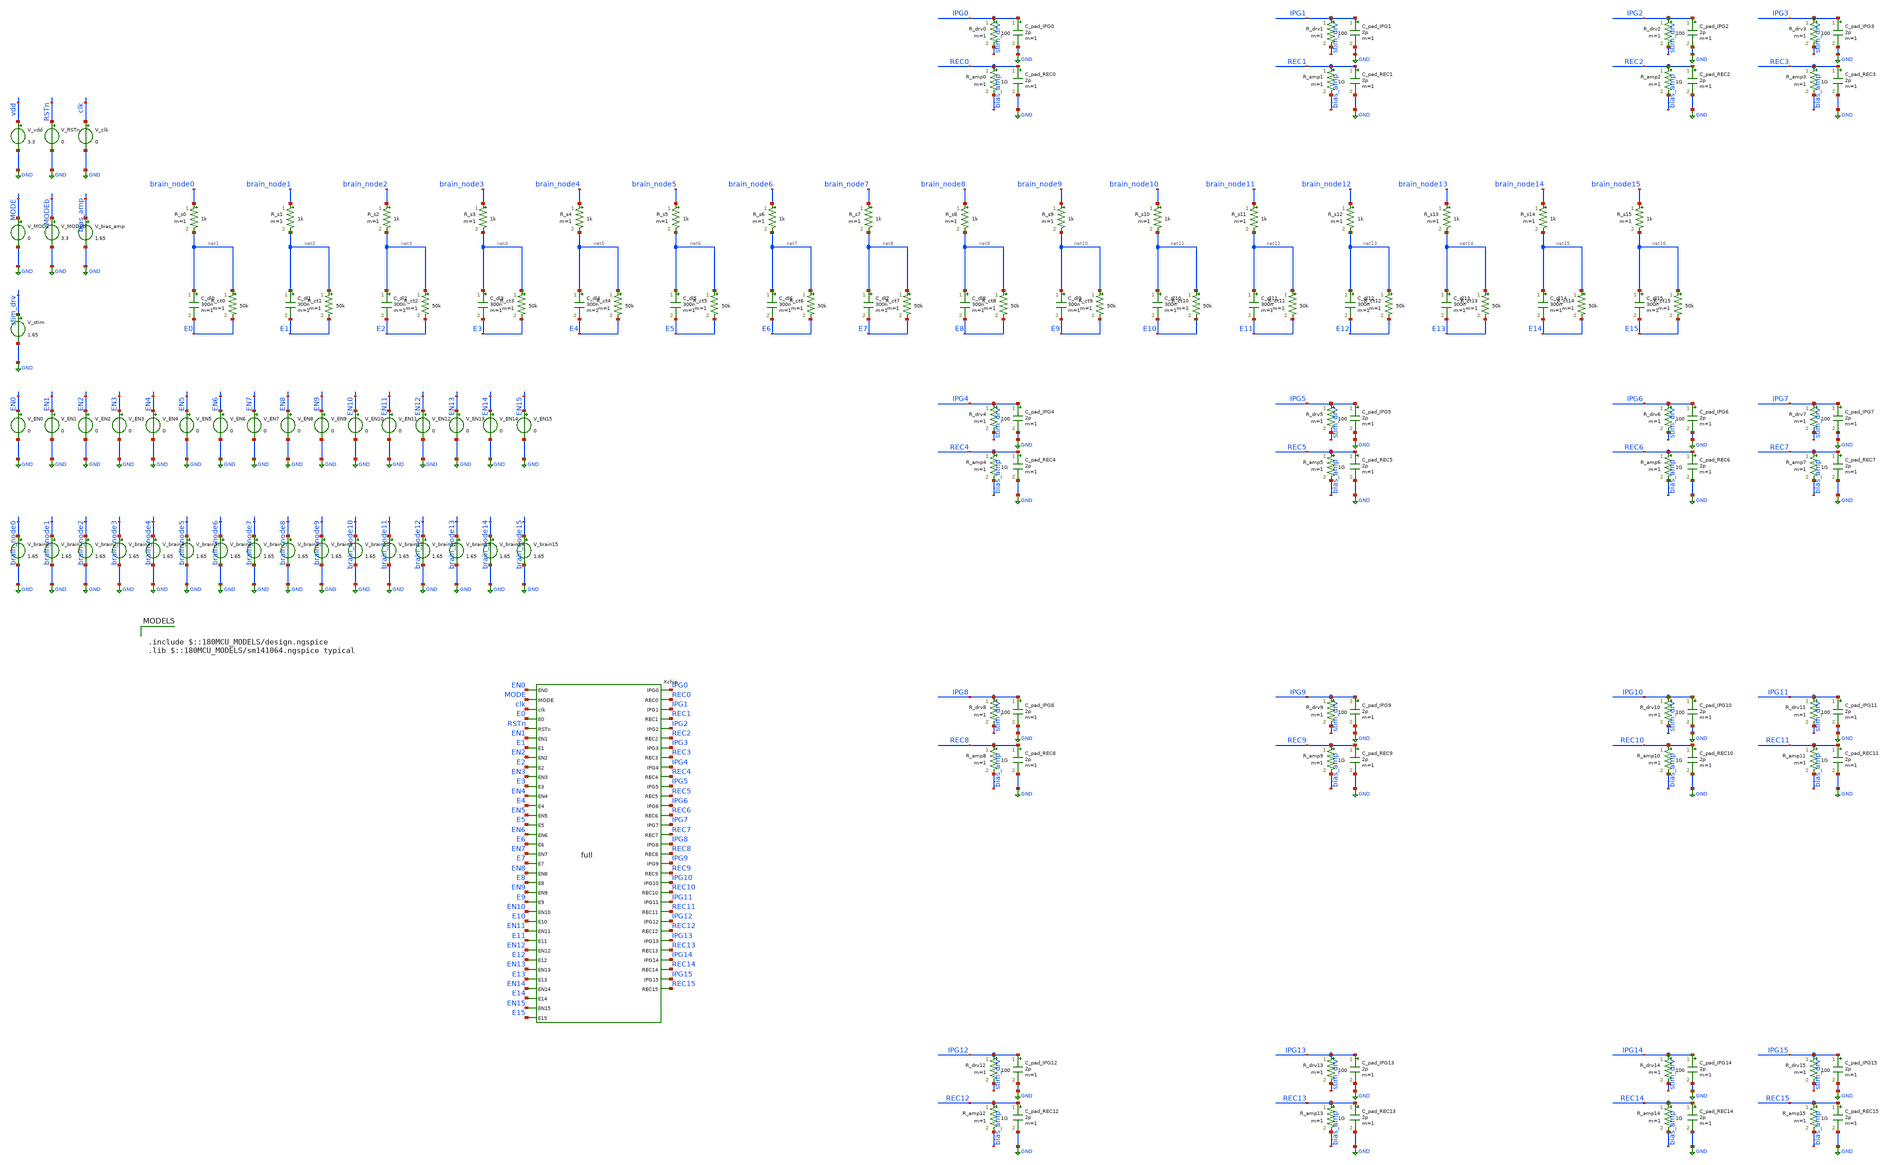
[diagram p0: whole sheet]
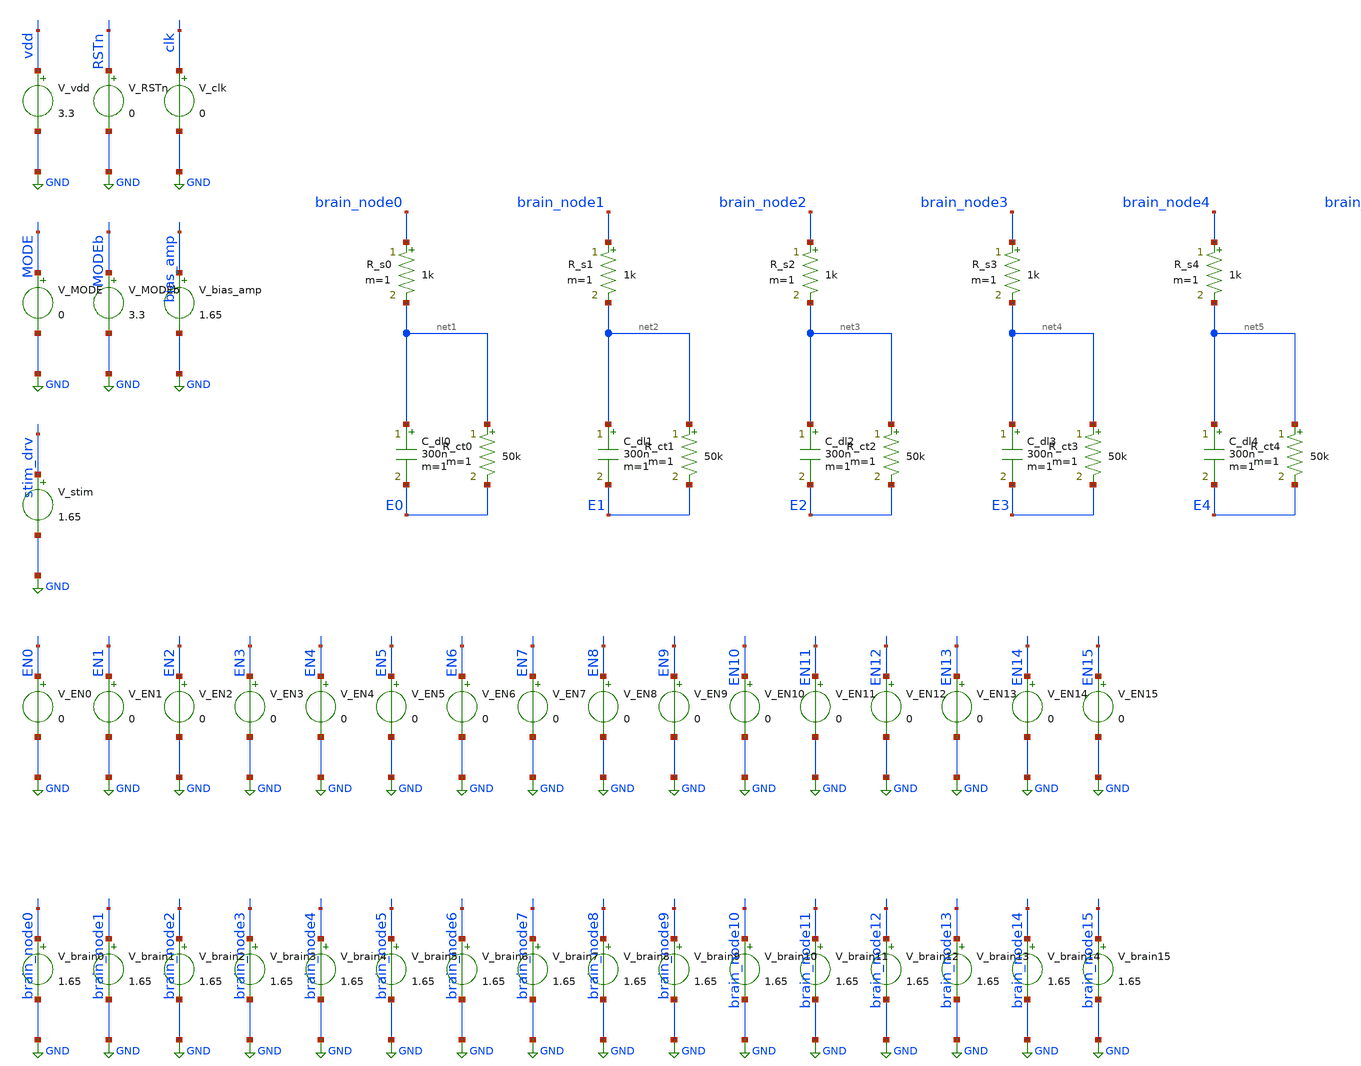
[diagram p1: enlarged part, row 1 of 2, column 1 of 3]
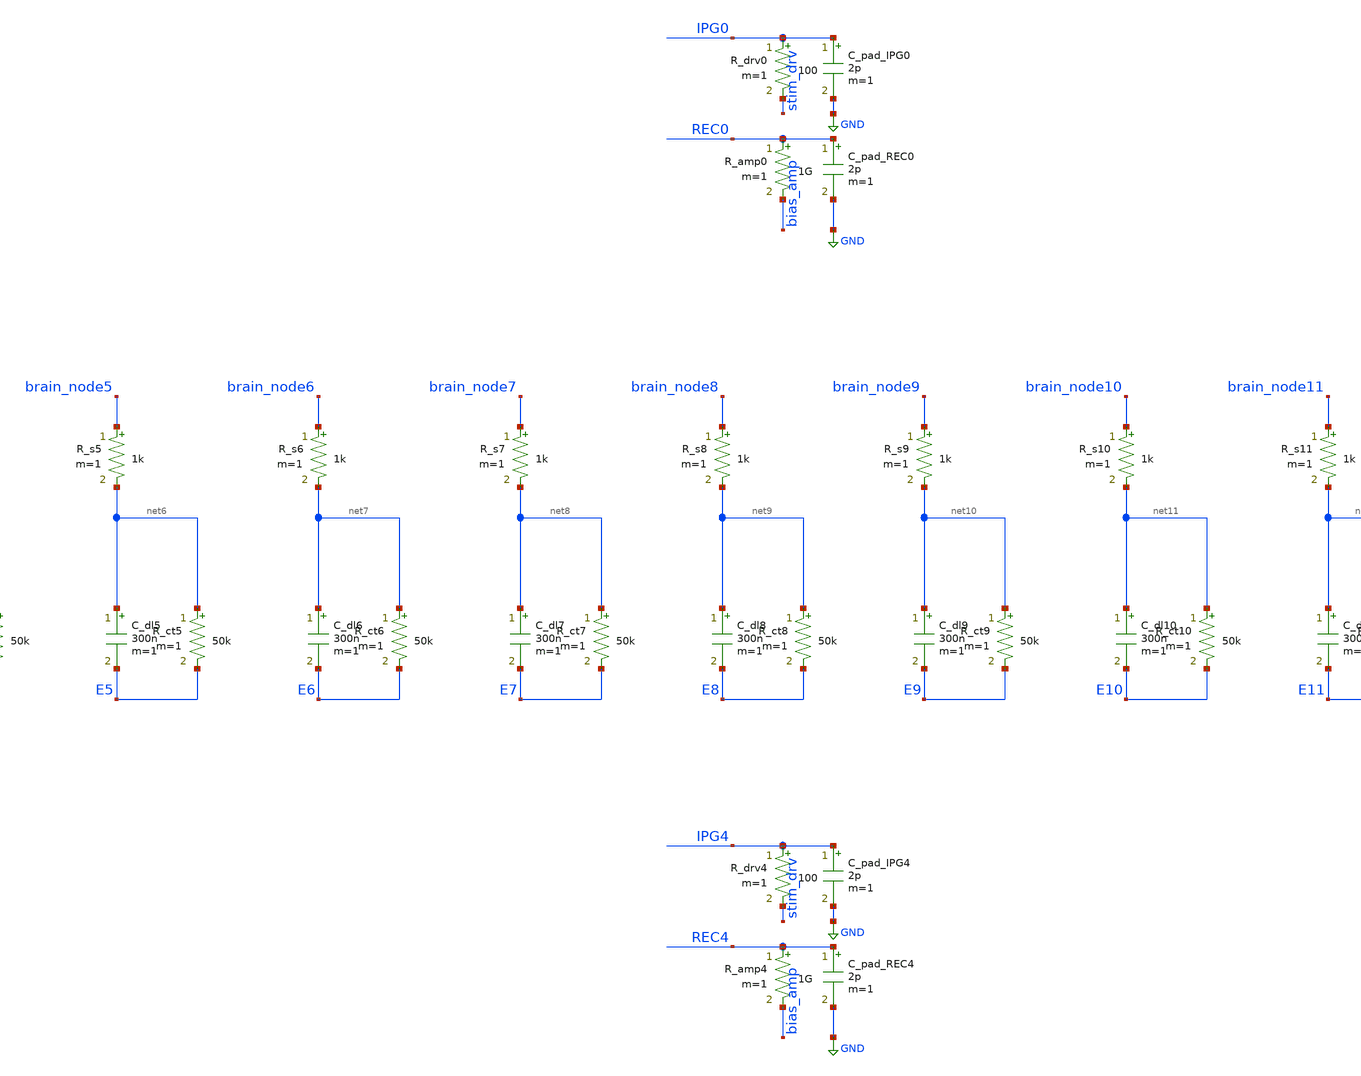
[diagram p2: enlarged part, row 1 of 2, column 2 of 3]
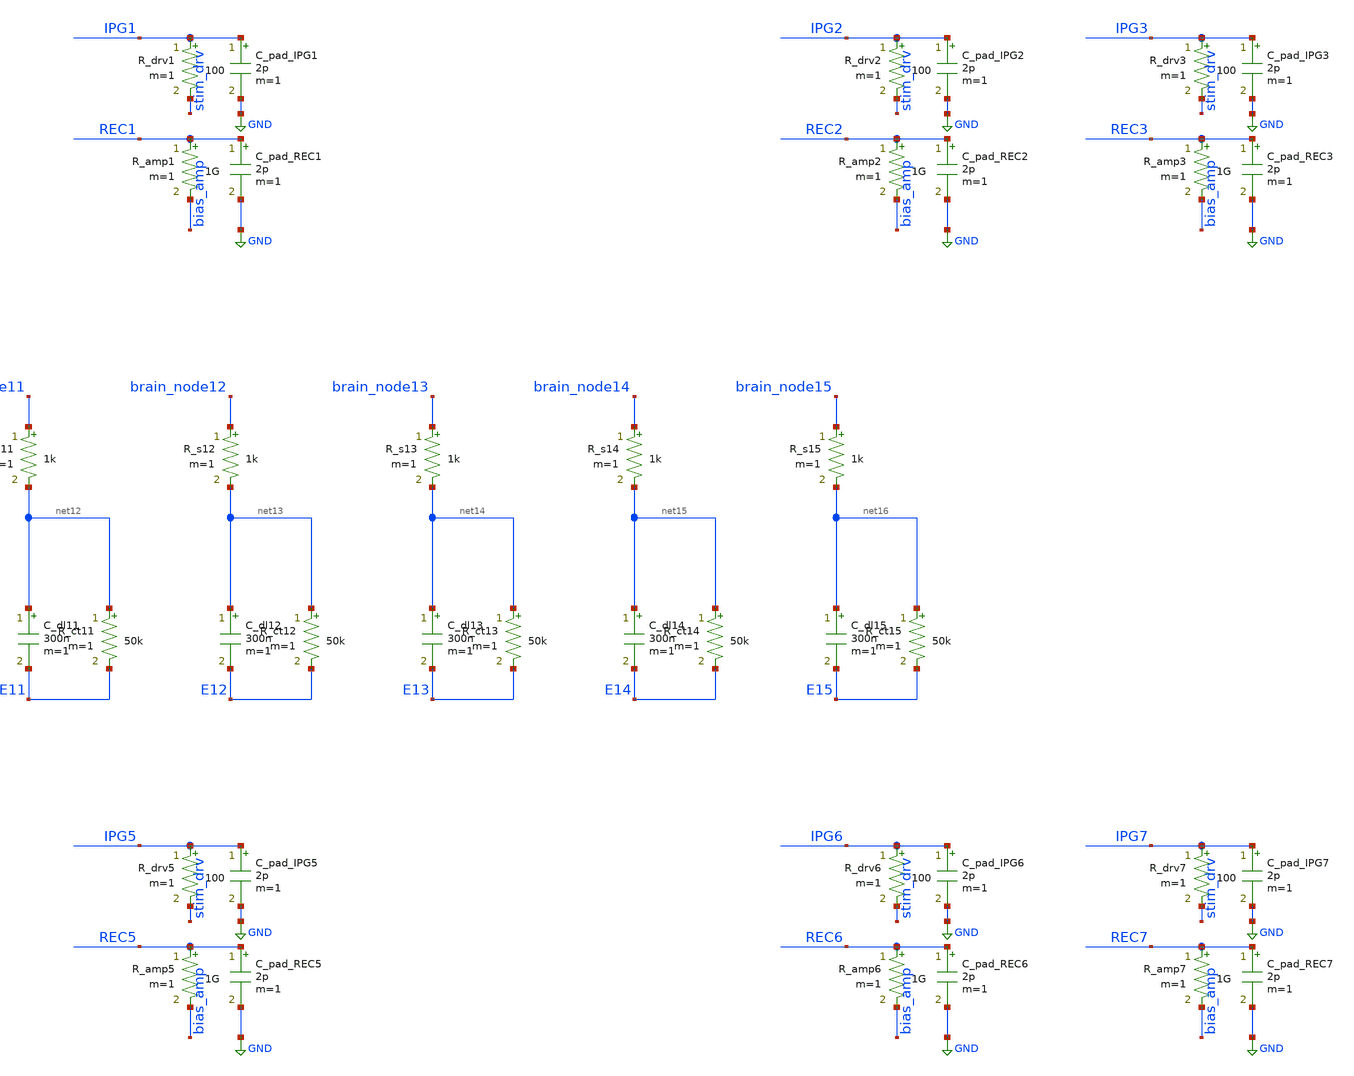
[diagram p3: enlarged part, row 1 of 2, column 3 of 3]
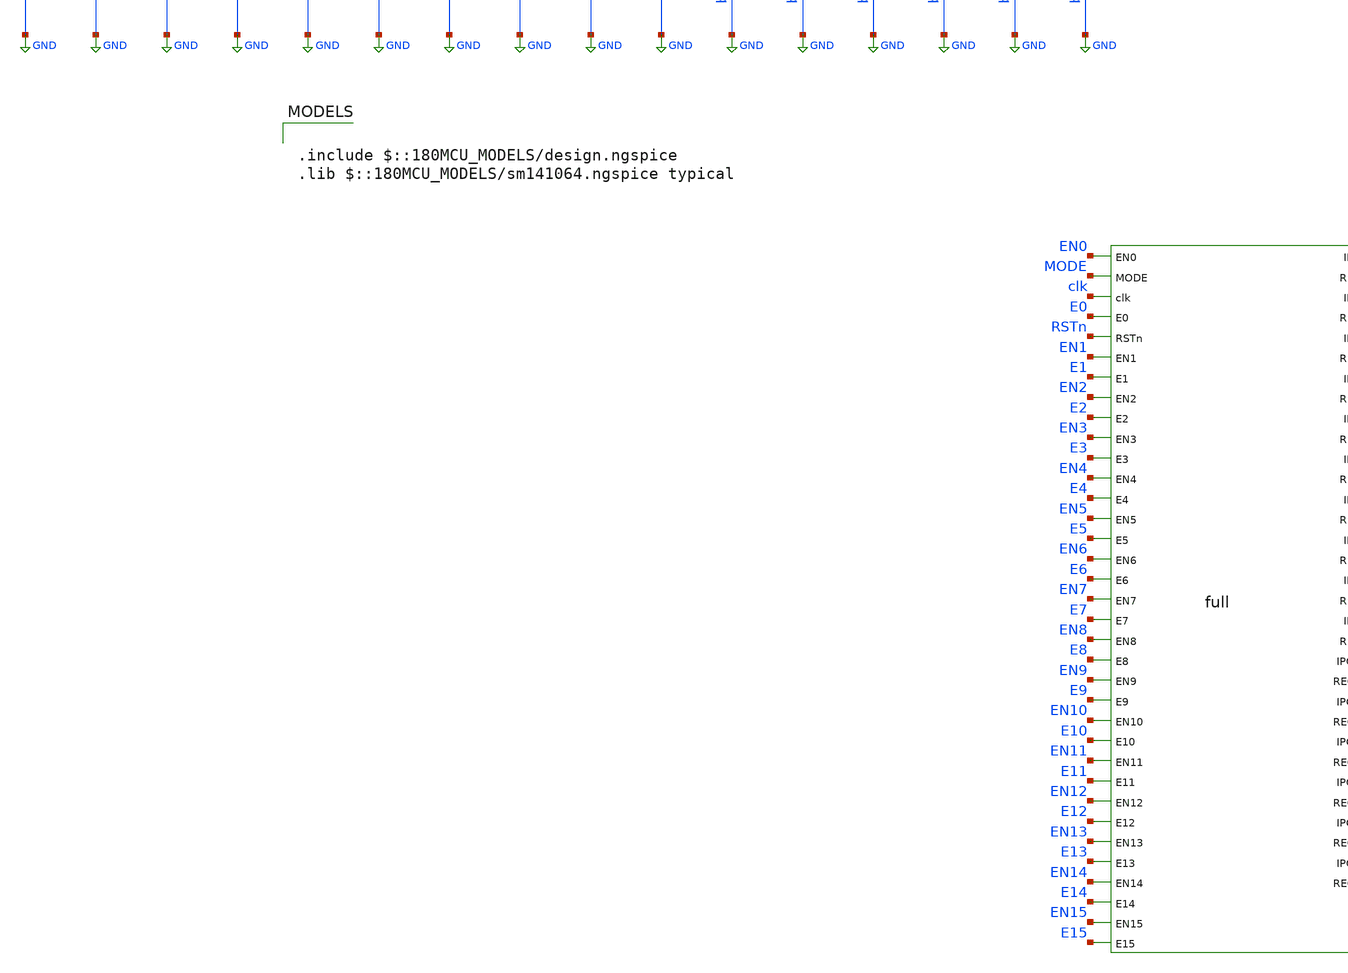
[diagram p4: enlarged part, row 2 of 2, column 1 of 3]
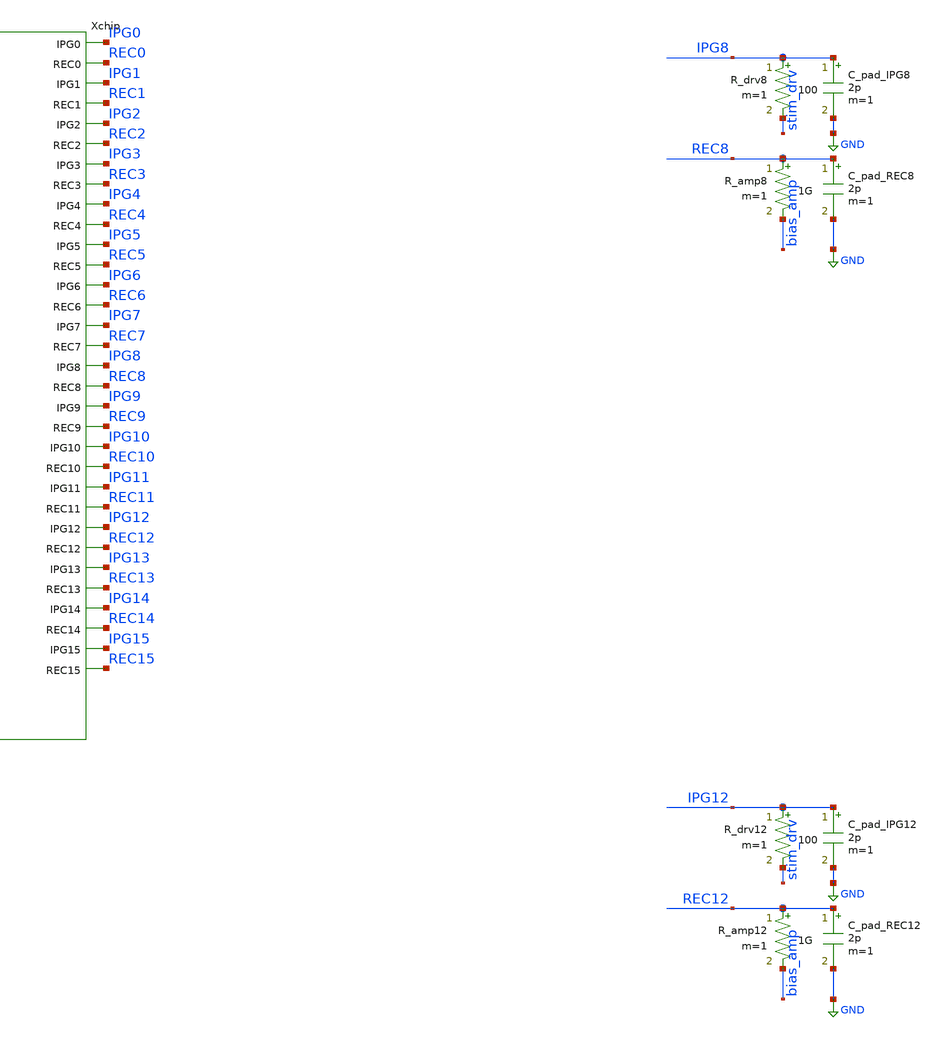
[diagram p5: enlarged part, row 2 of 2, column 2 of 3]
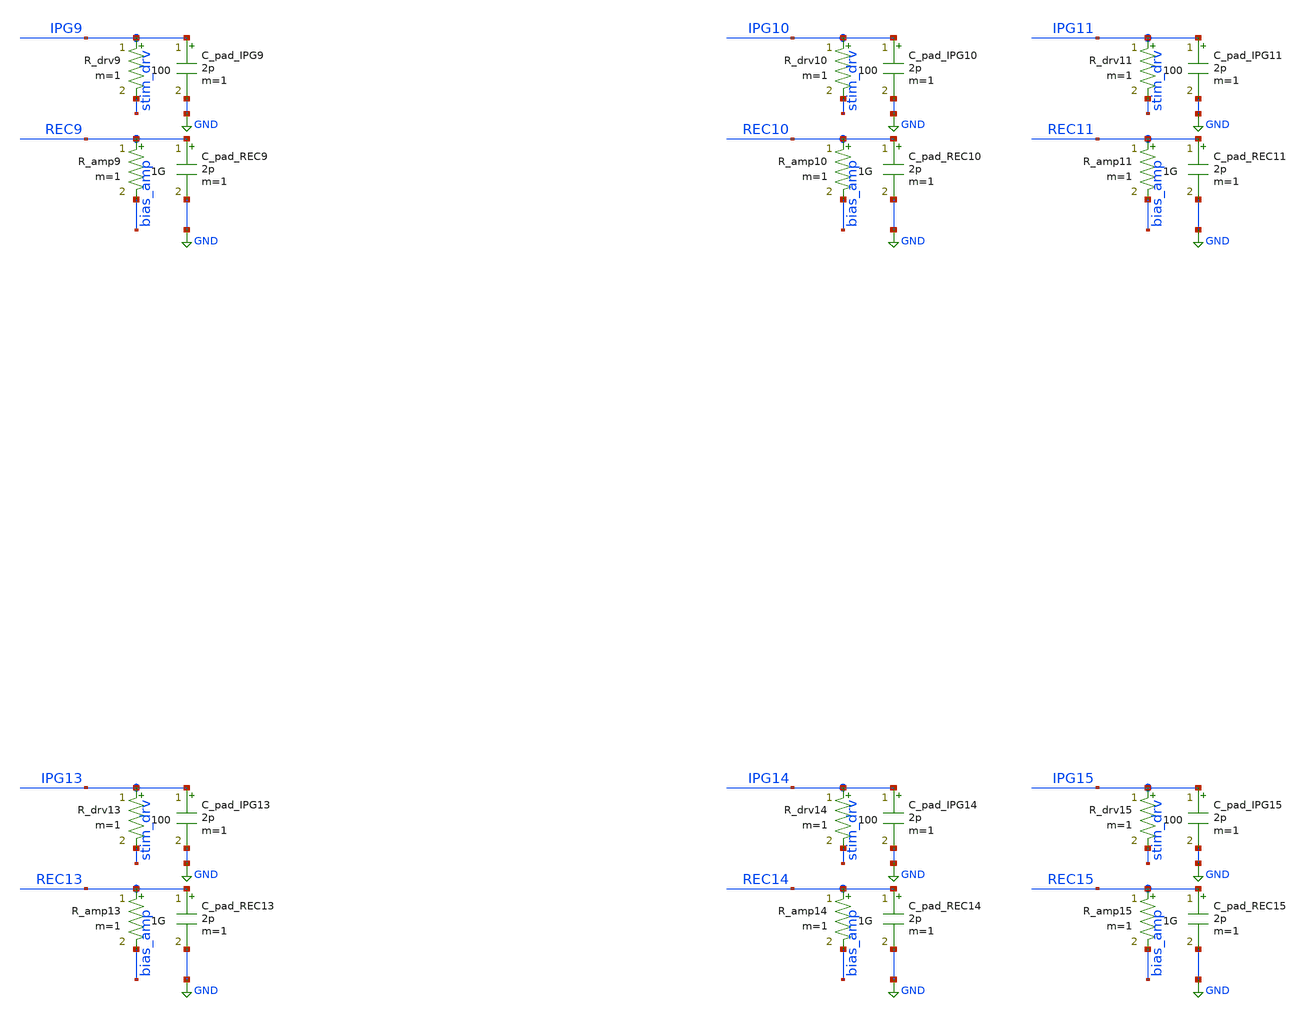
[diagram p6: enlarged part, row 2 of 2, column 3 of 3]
** sch_path: tb_realistic_16ch.sch
**.subckt tb_realistic_16ch
V_vdd vdd GND 3.3
V_RSTn RSTn GND 0
V_clk clk GND 0
V_MODE MODE GND 0
V_MODEb MODEb GND 3.3
V_bias_amp bias_amp GND 1.65
V_stim stim_drv GND 1.65
V_EN0 EN0 GND 0
V_EN1 EN1 GND 0
V_EN2 EN2 GND 0
V_EN3 EN3 GND 0
V_EN4 EN4 GND 0
V_EN5 EN5 GND 0
V_EN6 EN6 GND 0
V_EN7 EN7 GND 0
V_EN8 EN8 GND 0
V_EN9 EN9 GND 0
V_EN10 EN10 GND 0
V_EN11 EN11 GND 0
V_EN12 EN12 GND 0
V_EN13 EN13 GND 0
V_EN14 EN14 GND 0
V_EN15 EN15 GND 0
V_brain0 brain_node0 GND 1.65
V_brain1 brain_node1 GND 1.65
V_brain2 brain_node2 GND 1.65
V_brain3 brain_node3 GND 1.65
V_brain4 brain_node4 GND 1.65
V_brain5 brain_node5 GND 1.65
V_brain6 brain_node6 GND 1.65
V_brain7 brain_node7 GND 1.65
V_brain8 brain_node8 GND 1.65
V_brain9 brain_node9 GND 1.65
V_brain10 brain_node10 GND 1.65
V_brain11 brain_node11 GND 1.65
V_brain12 brain_node12 GND 1.65
V_brain13 brain_node13 GND 1.65
V_brain14 brain_node14 GND 1.65
V_brain15 brain_node15 GND 1.65
R_s0 brain_node0 net1 1k m=1
C_dl0 net1 E0 300n m=1
R_ct0 net1 E0 50k m=1
R_s1 brain_node1 net2 1k m=1
C_dl1 net2 E1 300n m=1
R_ct1 net2 E1 50k m=1
R_s2 brain_node2 net3 1k m=1
C_dl2 net3 E2 300n m=1
R_ct2 net3 E2 50k m=1
R_s3 brain_node3 net4 1k m=1
C_dl3 net4 E3 300n m=1
R_ct3 net4 E3 50k m=1
R_s4 brain_node4 net5 1k m=1
C_dl4 net5 E4 300n m=1
R_ct4 net5 E4 50k m=1
R_s5 brain_node5 net6 1k m=1
C_dl5 net6 E5 300n m=1
R_ct5 net6 E5 50k m=1
R_s6 brain_node6 net7 1k m=1
C_dl6 net7 E6 300n m=1
R_ct6 net7 E6 50k m=1
R_s7 brain_node7 net8 1k m=1
C_dl7 net8 E7 300n m=1
R_ct7 net8 E7 50k m=1
R_s8 brain_node8 net9 1k m=1
C_dl8 net9 E8 300n m=1
R_ct8 net9 E8 50k m=1
R_s9 brain_node9 net10 1k m=1
C_dl9 net10 E9 300n m=1
R_ct9 net10 E9 50k m=1
R_s10 brain_node10 net11 1k m=1
C_dl10 net11 E10 300n m=1
R_ct10 net11 E10 50k m=1
R_s11 brain_node11 net12 1k m=1
C_dl11 net12 E11 300n m=1
R_ct11 net12 E11 50k m=1
R_s12 brain_node12 net13 1k m=1
C_dl12 net13 E12 300n m=1
R_ct12 net13 E12 50k m=1
R_s13 brain_node13 net14 1k m=1
C_dl13 net14 E13 300n m=1
R_ct13 net14 E13 50k m=1
R_s14 brain_node14 net15 1k m=1
C_dl14 net15 E14 300n m=1
R_ct14 net15 E14 50k m=1
R_s15 brain_node15 net16 1k m=1
C_dl15 net16 E15 300n m=1
R_ct15 net16 E15 50k m=1
R_drv0 IPG0 stim_drv 100 m=1
C_pad_IPG0 IPG0 GND 2p m=1
R_amp0 REC0 bias_amp 1G m=1
C_pad_REC0 REC0 GND 2p m=1
R_drv1 IPG1 stim_drv 100 m=1
C_pad_IPG1 IPG1 GND 2p m=1
R_amp1 REC1 bias_amp 1G m=1
C_pad_REC1 REC1 GND 2p m=1
R_drv2 IPG2 stim_drv 100 m=1
C_pad_IPG2 IPG2 GND 2p m=1
R_amp2 REC2 bias_amp 1G m=1
C_pad_REC2 REC2 GND 2p m=1
R_drv3 IPG3 stim_drv 100 m=1
C_pad_IPG3 IPG3 GND 2p m=1
R_amp3 REC3 bias_amp 1G m=1
C_pad_REC3 REC3 GND 2p m=1
R_drv4 IPG4 stim_drv 100 m=1
C_pad_IPG4 IPG4 GND 2p m=1
R_amp4 REC4 bias_amp 1G m=1
C_pad_REC4 REC4 GND 2p m=1
R_drv5 IPG5 stim_drv 100 m=1
C_pad_IPG5 IPG5 GND 2p m=1
R_amp5 REC5 bias_amp 1G m=1
C_pad_REC5 REC5 GND 2p m=1
R_drv6 IPG6 stim_drv 100 m=1
C_pad_IPG6 IPG6 GND 2p m=1
R_amp6 REC6 bias_amp 1G m=1
C_pad_REC6 REC6 GND 2p m=1
R_drv7 IPG7 stim_drv 100 m=1
C_pad_IPG7 IPG7 GND 2p m=1
R_amp7 REC7 bias_amp 1G m=1
C_pad_REC7 REC7 GND 2p m=1
R_drv8 IPG8 stim_drv 100 m=1
C_pad_IPG8 IPG8 GND 2p m=1
R_amp8 REC8 bias_amp 1G m=1
C_pad_REC8 REC8 GND 2p m=1
R_drv9 IPG9 stim_drv 100 m=1
C_pad_IPG9 IPG9 GND 2p m=1
R_amp9 REC9 bias_amp 1G m=1
C_pad_REC9 REC9 GND 2p m=1
R_drv10 IPG10 stim_drv 100 m=1
C_pad_IPG10 IPG10 GND 2p m=1
R_amp10 REC10 bias_amp 1G m=1
C_pad_REC10 REC10 GND 2p m=1
R_drv11 IPG11 stim_drv 100 m=1
C_pad_IPG11 IPG11 GND 2p m=1
R_amp11 REC11 bias_amp 1G m=1
C_pad_REC11 REC11 GND 2p m=1
R_drv12 IPG12 stim_drv 100 m=1
C_pad_IPG12 IPG12 GND 2p m=1
R_amp12 REC12 bias_amp 1G m=1
C_pad_REC12 REC12 GND 2p m=1
R_drv13 IPG13 stim_drv 100 m=1
C_pad_IPG13 IPG13 GND 2p m=1
R_amp13 REC13 bias_amp 1G m=1
C_pad_REC13 REC13 GND 2p m=1
R_drv14 IPG14 stim_drv 100 m=1
C_pad_IPG14 IPG14 GND 2p m=1
R_amp14 REC14 bias_amp 1G m=1
C_pad_REC14 REC14 GND 2p m=1
R_drv15 IPG15 stim_drv 100 m=1
C_pad_IPG15 IPG15 GND 2p m=1
R_amp15 REC15 bias_amp 1G m=1
C_pad_REC15 REC15 GND 2p m=1
Xchip IPG0 EN0 MODE clk E0 REC0 RSTn IPG1 EN1 E1 REC1 IPG2 EN2 E2 REC2 IPG3 EN3 E3 REC3 IPG4 EN4 E4
+ REC4 IPG5 EN5 E5 REC5 IPG6 EN6 E6 REC6 IPG7 EN7 E7 REC7 IPG8 EN8 E8 REC8 IPG9 EN9 E9 REC9 IPG10 EN10 E10
+ REC10 IPG11 EN11 E11 REC11 IPG12 EN12 E12 REC12 IPG13 EN13 E13 REC13 IPG14 EN14 E14 REC14 IPG15 EN15 E15
+ REC15 full
**** begin user architecture code

.include $::180MCU_MODELS/design.ngspice
.lib $::180MCU_MODELS/sm141064.ngspice typical



.control
save all

** RSTn: low until 100ns then high
alter @V_RSTn[PWL] = [ 0 0  100n 0  100.001n 3.3  30m 3.3 ]

** Single latching clock pulse around 200ns
alter @V_clk[PWL] = [ 0 0  200n 0  200.001n 3.3  300n 3.3  300.001n 0  30m 0 ]

** EN[0..15]: all high after RSTn release
alter @V_EN0[PWL] = [ 0 0  150n 0  150.001n 3.3  30m 3.3 ]
alter @V_EN1[PWL] = [ 0 0  150n 0  150.001n 3.3  30m 3.3 ]
alter @V_EN2[PWL] = [ 0 0  150n 0  150.001n 3.3  30m 3.3 ]
alter @V_EN3[PWL] = [ 0 0  150n 0  150.001n 3.3  30m 3.3 ]
alter @V_EN4[PWL] = [ 0 0  150n 0  150.001n 3.3  30m 3.3 ]
alter @V_EN5[PWL] = [ 0 0  150n 0  150.001n 3.3  30m 3.3 ]
alter @V_EN6[PWL] = [ 0 0  150n 0  150.001n 3.3  30m 3.3 ]
alter @V_EN7[PWL] = [ 0 0  150n 0  150.001n 3.3  30m 3.3 ]
alter @V_EN8[PWL] = [ 0 0  150n 0  150.001n 3.3  30m 3.3 ]
alter @V_EN9[PWL] = [ 0 0  150n 0  150.001n 3.3  30m 3.3 ]
alter @V_EN10[PWL] = [ 0 0  150n 0  150.001n 3.3  30m 3.3 ]
alter @V_EN11[PWL] = [ 0 0  150n 0  150.001n 3.3  30m 3.3 ]
alter @V_EN12[PWL] = [ 0 0  150n 0  150.001n 3.3  30m 3.3 ]
alter @V_EN13[PWL] = [ 0 0  150n 0  150.001n 3.3  30m 3.3 ]
alter @V_EN14[PWL] = [ 0 0  150n 0  150.001n 3.3  30m 3.3 ]
alter @V_EN15[PWL] = [ 0 0  150n 0  150.001n 3.3  30m 3.3 ]

** MODE: stim phase 0-15ms (includes drain), record phase 15-30ms
alter @V_MODE[PWL]  = [ 0 0    15m 0    15.0001m 3.3   30m 3.3 ]
alter @V_MODEb[PWL] = [ 0 3.3  15m 3.3  15.0001m 0     30m 0 ]

** Brain LFPs: 100uV (10mV in source units, see scaling) 1kHz sines on 1.65V mid-rail,
** with 22.5deg phase increments per channel so REC traces are visually distinguishable.
alter @V_brain0[SIN] = [ 1.65 10m 1k 0 0 0.0000 ]
alter @V_brain1[SIN] = [ 1.65 10m 1k 0 0 22.5000 ]
alter @V_brain2[SIN] = [ 1.65 10m 1k 0 0 45.0000 ]
alter @V_brain3[SIN] = [ 1.65 10m 1k 0 0 67.5000 ]
alter @V_brain4[SIN] = [ 1.65 10m 1k 0 0 90.0000 ]
alter @V_brain5[SIN] = [ 1.65 10m 1k 0 0 112.5000 ]
alter @V_brain6[SIN] = [ 1.65 10m 1k 0 0 135.0000 ]
alter @V_brain7[SIN] = [ 1.65 10m 1k 0 0 157.5000 ]
alter @V_brain8[SIN] = [ 1.65 10m 1k 0 0 180.0000 ]
alter @V_brain9[SIN] = [ 1.65 10m 1k 0 0 202.5000 ]
alter @V_brain10[SIN] = [ 1.65 10m 1k 0 0 225.0000 ]
alter @V_brain11[SIN] = [ 1.65 10m 1k 0 0 247.5000 ]
alter @V_brain12[SIN] = [ 1.65 10m 1k 0 0 270.0000 ]
alter @V_brain13[SIN] = [ 1.65 10m 1k 0 0 292.5000 ]
alter @V_brain14[SIN] = [ 1.65 10m 1k 0 0 315.0000 ]
alter @V_brain15[SIN] = [ 1.65 10m 1k 0 0 337.5000 ]

** Stim driver: biphasic pulses at 0.5/1.5/2.5/3.5/4.5 ms during stim phase,
** then held at mid-rail for 10 ms drain before MODE switches.
alter @V_stim[PWL] = [  0          1.65  500u       1.65  500.001u   0.65  600u       0.65  600.001u
+   2.65  700u       2.65  700.001u   1.65  1500u      1.65  1500.001u  0.65  1600u      0.65  1600.001u
+  2.65  1700u      2.65  1700.001u  1.65  2500u      1.65  2500.001u  0.65  2600u      0.65  2600.001u
+  2.65  2700u      2.65  2700.001u  1.65  3500u      1.65  3500.001u  0.65  3600u      0.65  3600.001u
+  2.65  3700u      2.65  3700.001u  1.65  4500u      1.65  4500.001u  0.65  4600u      0.65  4600.001u
+  2.65  4700u      2.65  4700.001u  1.65  30m        1.65 ]

tran 1u 30m 0 5u

** plots
set color0 = white
set nolegend

** Plot a representative 4 channels (0,4,8,12): MODE marker, REC traces, E traces, scaled IPG traces
plot (v(MODE)*16.65/3.3)+0.825 v(REC0) v(REC1)+1 v(REC2)+2 v(REC3)+3 v(REC4)+4 v(REC5)+5 v(REC6)+6
+ v(REC7)+7 v(REC8)+8 v(REC9)+9 v(REC10)+10 v(REC11)+11 v(REC12)+12 v(REC13)+13 v(REC14)+14 v(REC15)+15 v(E0)
+ v(E1)+1 v(E2)+2 v(E3)+3 v(E4)+4 v(E5)+5 v(E6)+6 v(E7)+7 v(E8)+8 v(E9)+9 v(E10)+10 v(E11)+11 v(E12)+12
+ v(E13)+13 v(E14)+14 v(E15)+15 v(IPG0)/3+(1.65-1.65/3) (v(IPG1)/3+(1.65-1.65/3))+1 (v(IPG2)/3+(1.65-1.65/3))+2
+ (v(IPG3)/3+(1.65-1.65/3))+3 (v(IPG4)/3+(1.65-1.65/3))+4 (v(IPG5)/3+(1.65-1.65/3))+5 (v(IPG6)/3+(1.65-1.65/3))+6
+ (v(IPG7)/3+(1.65-1.65/3))+7 (v(IPG8)/3+(1.65-1.65/3))+8 (v(IPG9)/3+(1.65-1.65/3))+9 (v(IPG10)/3+(1.65-1.65/3))+10
+ (v(IPG11)/3+(1.65-1.65/3))+11 (v(IPG12)/3+(1.65-1.65/3))+12 (v(IPG13)/3+(1.65-1.65/3))+13 (v(IPG14)/3+(1.65-1.65/3))+14
+ (v(IPG15)/3+(1.65-1.65/3))+15
plot v(REC0) v(REC1)+0.1 v(REC2)+0.2 v(REC3)+0.3 v(REC4)+0.4 v(REC5)+0.5 v(REC6)+0.6 v(REC7)+0.7
+ v(REC8)+0.8 v(REC9)+0.9 v(REC10)+1 v(REC11)+1.1 v(REC12)+1.2 v(REC13)+1.3 v(REC14)+1.4 v(REC15)+1.5 v(E0)
+ v(E1)+0.1 v(E2)+0.2 v(E3)+0.3 v(E4)+0.4 v(E5)+0.5 v(E6)+0.6 v(E7)+0.7 v(E8)+0.8 v(E9)+0.9 v(E10)+1 v(E11)+1.1
+ v(E12)+1.2 v(E13)+1.3 v(E14)+1.4 v(E15)+1.5 v(IPG0)/3+(1.65-1.65/3) (v(IPG1)/3+(1.65-1.65/3))+0.1
+ (v(IPG2)/3+(1.65-1.65/3))+0.2 (v(IPG3)/3+(1.65-1.65/3))+0.3 (v(IPG4)/3+(1.65-1.65/3))+0.4 (v(IPG5)/3+(1.65-1.65/3))+0.5
+ (v(IPG6)/3+(1.65-1.65/3))+0.6 (v(IPG7)/3+(1.65-1.65/3))+0.7 (v(IPG8)/3+(1.65-1.65/3))+0.8 (v(IPG9)/3+(1.65-1.65/3))+0.9
+ (v(IPG10)/3+(1.65-1.65/3))+1 (v(IPG11)/3+(1.65-1.65/3))+1.1 (v(IPG12)/3+(1.65-1.65/3))+1.2 (v(IPG13)/3+(1.65-1.65/3))+1.3
+ (v(IPG14)/3+(1.65-1.65/3))+1.4 (v(IPG15)/3+(1.65-1.65/3))+1.5 xlimit 14m 30m ylimit 1.6 3.2
plot v(REC0) v(REC1)+1 v(REC2)+2 v(REC3)+3 v(REC4)+4 v(REC5)+5 v(REC6)+6 v(REC7)+7 v(REC8)+8
+ v(REC9)+9 v(REC10)+10 v(REC11)+11 v(REC12)+12 v(REC13)+13 v(REC14)+14 v(REC15)+15 v(E0) v(E1)+1 v(E2)+2
+ v(E3)+3 v(E4)+4 v(E5)+5 v(E6)+6 v(E7)+7 v(E8)+8 v(E9)+9 v(E10)+10 v(E11)+11 v(E12)+12 v(E13)+13 v(E14)+14
+ v(E15)+15 v(IPG0)/3+(1.65-1.65/3) (v(IPG1)/3+(1.65-1.65/3))+1 (v(IPG2)/3+(1.65-1.65/3))+2
+ (v(IPG3)/3+(1.65-1.65/3))+3 (v(IPG4)/3+(1.65-1.65/3))+4 (v(IPG5)/3+(1.65-1.65/3))+5 (v(IPG6)/3+(1.65-1.65/3))+6
+ (v(IPG7)/3+(1.65-1.65/3))+7 (v(IPG8)/3+(1.65-1.65/3))+8 (v(IPG9)/3+(1.65-1.65/3))+9 (v(IPG10)/3+(1.65-1.65/3))+10
+ (v(IPG11)/3+(1.65-1.65/3))+11 (v(IPG12)/3+(1.65-1.65/3))+12 (v(IPG13)/3+(1.65-1.65/3))+13 (v(IPG14)/3+(1.65-1.65/3))+14
+ (v(IPG15)/3+(1.65-1.65/3))+15 xlimit 0m 5m
write tb_realistic_16ch.raw
.endc


**** end user architecture code
**.ends
.GLOBAL GND
.end
